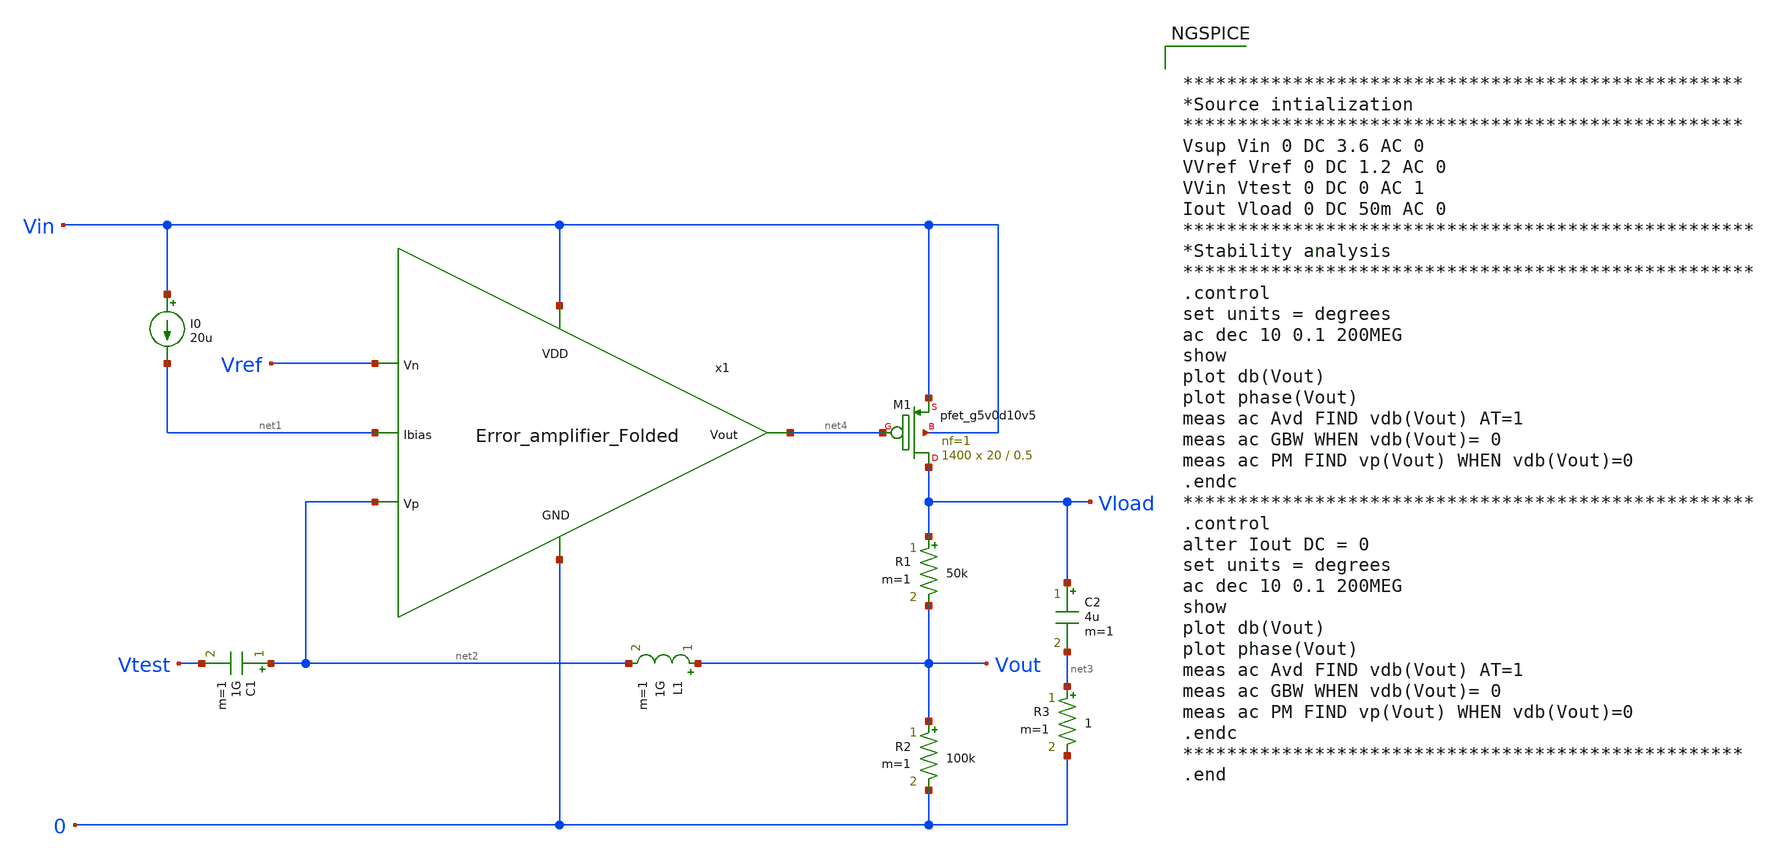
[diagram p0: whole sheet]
** sch_path: Analog_Blocks/LDO/Testbench/LDO_test_stability_TB.sch
**.subckt LDO_test_stability_TB
XM1 Vload net4 Vin Vin sky130_fd_pr__pfet_g5v0d10v5 L=0.5 W=20 nf=1 ad='int((nf+1)/2) * W/nf * 0.29'
+ as='int((nf+2)/2) * W/nf * 0.29' pd='2*int((nf+1)/2) * (W/nf + 0.29)' ps='2*int((nf+2)/2) * (W/nf + 0.29)'
+ nrd='0.29 / W' nrs='0.29 / W' sa=0 sb=0 sd=0 mult=1400 m=1400
R1 Vload Vout 50k m=1
R2 Vout 0 100k m=1
I0 Vin net1 20u
L1 Vout net2 1G m=1
C1 net2 Vtest 1G m=1
C2 Vload net3 4u m=1
R3 net3 0 1 m=1
x1 Vin net4 net2 Vref net1 0 Error_amplifier_Folded
**** begin user architecture code


***************************************************
*Source intialization
***************************************************
Vsup Vin 0 DC 3.6 AC 0
VVref Vref 0 DC 1.2 AC 0
VVin Vtest 0 DC 0 AC 1
Iout Vload 0 DC 50m AC 0
****************************************************
*Stability analysis
****************************************************
.control
set units = degrees
ac dec 10 0.1 200MEG
show
plot db(Vout)
plot phase(Vout)
meas ac Avd FIND vdb(Vout) AT=1
meas ac GBW WHEN vdb(Vout)= 0
meas ac PM FIND vp(Vout) WHEN vdb(Vout)=0
.endc
****************************************************
.control
alter Iout DC = 0
set units = degrees
ac dec 10 0.1 200MEG
show
plot db(Vout)
plot phase(Vout)
meas ac Avd FIND vdb(Vout) AT=1
meas ac GBW WHEN vdb(Vout)= 0
meas ac PM FIND vp(Vout) WHEN vdb(Vout)=0
.endc
***************************************************
.end




.param mc_mm_switch=0
.param mc_pr_switch=0
.include ~/mabrains/Analog_blocks/models/sky130A/libs.ref/sky130_fd_pr/spice/sky130_fd_pr__nfet_01v8__sf.corner.spice
.include ~/mabrains/Analog_blocks/models/sky130A/libs.ref/sky130_fd_pr/spice/sky130_fd_pr__nfet_01v8_lvt__sf.corner.spice
.include ~/mabrains/Analog_blocks/models/sky130A/libs.ref/sky130_fd_pr/spice/sky130_fd_pr__pfet_01v8__sf.corner.spice
.include ~/mabrains/Analog_blocks/models/sky130A/libs.ref/sky130_fd_pr/spice/sky130_fd_pr__nfet_03v3_nvt__sf.corner.spice
.include ~/mabrains/Analog_blocks/models/sky130A/libs.ref/sky130_fd_pr/spice/sky130_fd_pr__nfet_05v0_nvt__sf.corner.spice
.include ~/mabrains/Analog_blocks/models/sky130A/libs.ref/sky130_fd_pr/spice/sky130_fd_pr__esd_nfet_01v8__sf.corner.spice
.include ~/mabrains/Analog_blocks/models/sky130A/libs.ref/sky130_fd_pr/spice/sky130_fd_pr__pfet_01v8_lvt__sf.corner.spice
.include ~/mabrains/Analog_blocks/models/sky130A/libs.ref/sky130_fd_pr/spice/sky130_fd_pr__pfet_01v8_hvt__sf.corner.spice
.include ~/mabrains/Analog_blocks/models/sky130A/libs.ref/sky130_fd_pr/spice/sky130_fd_pr__esd_pfet_g5v0d10v5__sf.corner.spice
.include ~/mabrains/Analog_blocks/models/sky130A/libs.ref/sky130_fd_pr/spice/sky130_fd_pr__pfet_g5v0d10v5__sf.corner.spice
.include ~/mabrains/Analog_blocks/models/sky130A/libs.ref/sky130_fd_pr/spice/sky130_fd_pr__pfet_g5v0d16v0__sf.corner.spice
.include ~/mabrains/Analog_blocks/models/sky130A/libs.ref/sky130_fd_pr/spice/sky130_fd_pr__nfet_g5v0d10v5__sf.corner.spice
.include ~/mabrains/Analog_blocks/models/sky130A/libs.ref/sky130_fd_pr/spice/sky130_fd_pr__nfet_g5v0d16v0__sf_discrete.corner.spice
.include ~/mabrains/Analog_blocks/models/sky130A/libs.ref/sky130_fd_pr/spice/sky130_fd_pr__esd_nfet_g5v0d10v5__sf.corner.spice
.include ~/mabrains/Analog_blocks/models/sky130A/libs.ref/sky130_fd_pr/spice/sky130_fd_pr__pfet_20v0__sf_discrete.corner.spice
.include ~/mabrains/Analog_blocks/models/sky130A/libs.ref/sky130_fd_pr/spice/sky130_fd_pr__nfet_20v0__sf_discrete.corner.spice
.include ~/mabrains/Analog_blocks/models/sky130A/libs.tech/ngspice/corners/sf/nonfet.spice
* Mismatch parameters
.include ~/mabrains/Analog_blocks/models/sky130A/libs.ref/sky130_fd_pr/spice/sky130_fd_pr__nfet_01v8__mismatch.corner.spice
.include ~/mabrains/Analog_blocks/models/sky130A/libs.ref/sky130_fd_pr/spice/sky130_fd_pr__pfet_01v8__mismatch.corner.spice
.include ~/mabrains/Analog_blocks/models/sky130A/libs.ref/sky130_fd_pr/spice/sky130_fd_pr__nfet_01v8_lvt__mismatch.corner.spice
.include ~/mabrains/Analog_blocks/models/sky130A/libs.ref/sky130_fd_pr/spice/sky130_fd_pr__pfet_01v8_lvt__mismatch.corner.spice
.include ~/mabrains/Analog_blocks/models/sky130A/libs.ref/sky130_fd_pr/spice/sky130_fd_pr__pfet_01v8_hvt__mismatch.corner.spice
.include ~/mabrains/Analog_blocks/models/sky130A/libs.ref/sky130_fd_pr/spice/sky130_fd_pr__nfet_g5v0d10v5__mismatch.corner.spice
.include ~/mabrains/Analog_blocks/models/sky130A/libs.ref/sky130_fd_pr/spice/sky130_fd_pr__pfet_g5v0d10v5__mismatch.corner.spice
.include ~/mabrains/Analog_blocks/models/sky130A/libs.ref/sky130_fd_pr/spice/sky130_fd_pr__nfet_05v0_nvt__mismatch.corner.spice
.include ~/mabrains/Analog_blocks/models/sky130A/libs.ref/sky130_fd_pr/spice/sky130_fd_pr__nfet_03v3_nvt__mismatch.corner.spice
* Resistor/Capacitor
.include ~/mabrains/Analog_blocks/models/sky130A/libs.tech/ngspice/r+c/res_typical__cap_typical.spice
.include ~/mabrains/Analog_blocks/models/sky130A/libs.tech/ngspice/r+c/res_typical__cap_typical__lin.spice
* Special cells
.include ~/mabrains/Analog_blocks/models/sky130A/libs.tech/ngspice/corners/sf/specialized_cells.spice
* All models
.include ~/mabrains/Analog_blocks/models/sky130A/libs.tech/ngspice/all.spice
* Corner
.include ~/mabrains/Analog_blocks/models/sky130A/libs.tech/ngspice/corners/sf/rf.spice



**** end user architecture code
**.ends

* expanding   symbol:
*+  /home/eslam/mabrains/Analog_blocks/Analog_Blocks/LDO/Schematic/LDO_Folded_1.8v/Error_amplifier_Folded.sym # of pins=6
** sym_path: Analog_Blocks/LDO/Schematic/LDO_Folded_1.8v/Error_amplifier_Folded.sym
** sch_path: Analog_Blocks/LDO/Schematic/LDO_Folded_1.8v/Error_amplifier_Folded.sch
.subckt Error_amplifier_Folded VDD Vout Vp Vn Ibias GND
*.ipin VDD
*.ipin GND
*.ipin Vp
*.ipin Vn
*.opin Vout
*.ipin Ibias
XM1 net3 Vp net1 GND sky130_fd_pr__nfet_g5v0d10v5 L=0.5 W=50 nf=1 ad='int((nf+1)/2) * W/nf * 0.29' as='int((nf+2)/2) * W/nf * 0.29'
+ pd='2*int((nf+1)/2) * (W/nf + 0.29)' ps='2*int((nf+2)/2) * (W/nf + 0.29)' nrd='0.29 / W' nrs='0.29 / W'
+ sa=0 sb=0 sd=0 mult=1 m=1
XM2 net2 Vn net1 GND sky130_fd_pr__nfet_g5v0d10v5 L=0.5 W=50 nf=1 ad='int((nf+1)/2) * W/nf * 0.29' as='int((nf+2)/2) * W/nf * 0.29'
+ pd='2*int((nf+1)/2) * (W/nf + 0.29)' ps='2*int((nf+2)/2) * (W/nf + 0.29)' nrd='0.29 / W' nrs='0.29 / W'
+ sa=0 sb=0 sd=0 mult=1 m=1
XM9 Vout net4 GND GND sky130_fd_pr__nfet_g5v0d10v5 L=2 W=6 nf=1 ad='int((nf+1)/2) * W/nf * 0.29' as='int((nf+2)/2) * W/nf * 0.29'
+ pd='2*int((nf+1)/2) * (W/nf + 0.29)' ps='2*int((nf+2)/2) * (W/nf + 0.29)' nrd='0.29 / W' nrs='0.29 / W'
+ sa=0 sb=0 sd=0 mult=1 m=1
XM6 net4 net6 net3 VDD sky130_fd_pr__pfet_g5v0d10v5 L=0.5 W=40 nf=1 ad='int((nf+1)/2) * W/nf * 0.29'
+ as='int((nf+2)/2) * W/nf * 0.29' pd='2*int((nf+1)/2) * (W/nf + 0.29)' ps='2*int((nf+2)/2) * (W/nf + 0.29)'
+ nrd='0.29 / W' nrs='0.29 / W' sa=0 sb=0 sd=0 mult=1 m=1
XM5 net2 net5 VDD VDD sky130_fd_pr__pfet_g5v0d10v5 L=0.5 W=40 nf=1 ad='int((nf+1)/2) * W/nf * 0.29' as='int((nf+2)/2) * W/nf * 0.29'
+ pd='2*int((nf+1)/2) * (W/nf + 0.29)' ps='2*int((nf+2)/2) * (W/nf + 0.29)' nrd='0.29 / W' nrs='0.29 / W'
+ sa=0 sb=0 sd=0 mult=1 m=1
XM4 net3 net5 VDD VDD sky130_fd_pr__pfet_g5v0d10v5 L=0.5 W=40 nf=1 ad='int((nf+1)/2) * W/nf * 0.29' as='int((nf+2)/2) * W/nf * 0.29'
+ pd='2*int((nf+1)/2) * (W/nf + 0.29)' ps='2*int((nf+2)/2) * (W/nf + 0.29)' nrd='0.29 / W' nrs='0.29 / W'
+ sa=0 sb=0 sd=0 mult=1 m=1
XM3 net1 Ibias GND GND sky130_fd_pr__nfet_g5v0d10v5 L=0.9 W=12 nf=1 ad='int((nf+1)/2) * W/nf * 0.29'
+ as='int((nf+2)/2) * W/nf * 0.29' pd='2*int((nf+1)/2) * (W/nf + 0.29)' ps='2*int((nf+2)/2) * (W/nf + 0.29)'
+ nrd='0.29 / W' nrs='0.29 / W' sa=0 sb=0 sd=0 mult=1 m=1
XM7 Vout net6 net2 VDD sky130_fd_pr__pfet_g5v0d10v5 L=0.5 W=40 nf=1 ad='int((nf+1)/2) * W/nf * 0.29'
+ as='int((nf+2)/2) * W/nf * 0.29' pd='2*int((nf+1)/2) * (W/nf + 0.29)' ps='2*int((nf+2)/2) * (W/nf + 0.29)'
+ nrd='0.29 / W' nrs='0.29 / W' sa=0 sb=0 sd=0 mult=1 m=1
XM8 net4 net4 GND GND sky130_fd_pr__nfet_g5v0d10v5 L=2 W=6 nf=1 ad='int((nf+1)/2) * W/nf * 0.29' as='int((nf+2)/2) * W/nf * 0.29'
+ pd='2*int((nf+1)/2) * (W/nf + 0.29)' ps='2*int((nf+2)/2) * (W/nf + 0.29)' nrd='0.29 / W' nrs='0.29 / W'
+ sa=0 sb=0 sd=0 mult=1 m=1
XM10 Ibias Ibias GND GND sky130_fd_pr__nfet_g5v0d10v5 L=0.9 W=12 nf=1 ad='int((nf+1)/2) * W/nf * 0.29'
+ as='int((nf+2)/2) * W/nf * 0.29' pd='2*int((nf+1)/2) * (W/nf + 0.29)' ps='2*int((nf+2)/2) * (W/nf + 0.29)'
+ nrd='0.29 / W' nrs='0.29 / W' sa=0 sb=0 sd=0 mult=1 m=1
XM11 net5 Ibias GND GND sky130_fd_pr__nfet_g5v0d10v5 L=0.9 W=6 nf=1 ad='int((nf+1)/2) * W/nf * 0.29'
+ as='int((nf+2)/2) * W/nf * 0.29' pd='2*int((nf+1)/2) * (W/nf + 0.29)' ps='2*int((nf+2)/2) * (W/nf + 0.29)'
+ nrd='0.29 / W' nrs='0.29 / W' sa=0 sb=0 sd=0 mult=1 m=1
XM12 net6 Ibias GND GND sky130_fd_pr__nfet_g5v0d10v5 L=0.9 W=6 nf=1 ad='int((nf+1)/2) * W/nf * 0.29'
+ as='int((nf+2)/2) * W/nf * 0.29' pd='2*int((nf+1)/2) * (W/nf + 0.29)' ps='2*int((nf+2)/2) * (W/nf + 0.29)'
+ nrd='0.29 / W' nrs='0.29 / W' sa=0 sb=0 sd=0 mult=1 m=1
XM13 net5 net5 VDD VDD sky130_fd_pr__pfet_g5v0d10v5 L=0.5 W=13.5 nf=1 ad='int((nf+1)/2) * W/nf * 0.29'
+ as='int((nf+2)/2) * W/nf * 0.29' pd='2*int((nf+1)/2) * (W/nf + 0.29)' ps='2*int((nf+2)/2) * (W/nf + 0.29)'
+ nrd='0.29 / W' nrs='0.29 / W' sa=0 sb=0 sd=0 mult=1 m=1
XM14 net6 net6 VDD VDD sky130_fd_pr__pfet_g5v0d10v5 L=1 W=2 nf=1 ad='int((nf+1)/2) * W/nf * 0.29' as='int((nf+2)/2) * W/nf * 0.29'
+ pd='2*int((nf+1)/2) * (W/nf + 0.29)' ps='2*int((nf+2)/2) * (W/nf + 0.29)' nrd='0.29 / W' nrs='0.29 / W'
+ sa=0 sb=0 sd=0 mult=1 m=1
.ends

.end
